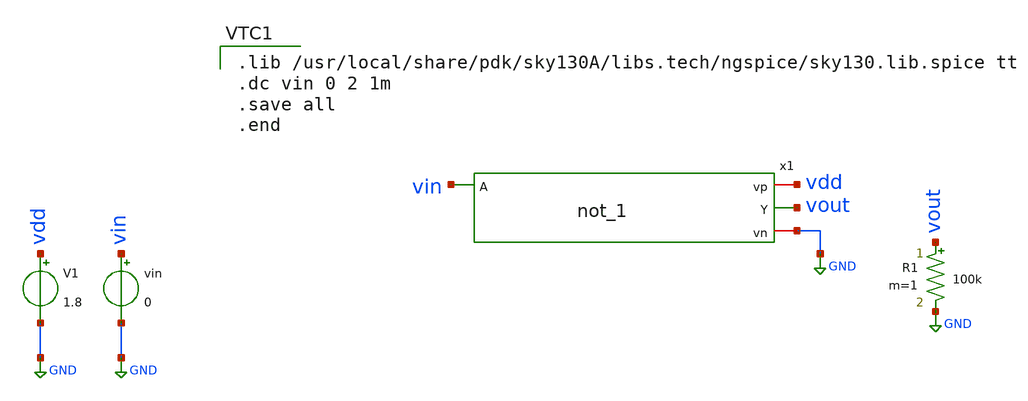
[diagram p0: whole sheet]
** sch_path: VLSI/PROVA_01/Simulazione postlayout/not_1_TB.sch
**.subckt not_1_TB
x1 vdd vin vout GND not_1
V1 vdd GND 1.8
vin vin GND 0
R1 vout GND 100k m=1
**** begin user architecture code

.lib /usr/local/share/pdk/sky130A/libs.tech/ngspice/sky130.lib.spice tt
.dc vin 0 2 1m
.save all
.end

**** end user architecture code
**.ends
.GLOBAL GND
.end
